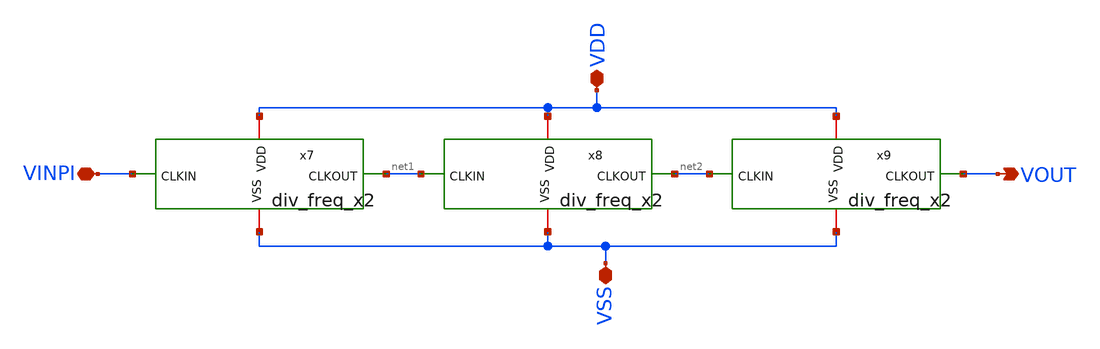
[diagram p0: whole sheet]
** sch_path: design/blocks-std-custom/div_freq_x8/schematic/div_freq_x8.sch
**.subckt div_freq_x8 VDD VSS VINPI VOUT
*.iopin VDD
*.iopin VSS
*.iopin VINPI
*.opin VOUT
x7 VDD VSS net1 VINPI div_freq_x2
x8 VDD VSS net2 net1 div_freq_x2
x9 VDD VSS VOUT net2 div_freq_x2
**.ends
.end
